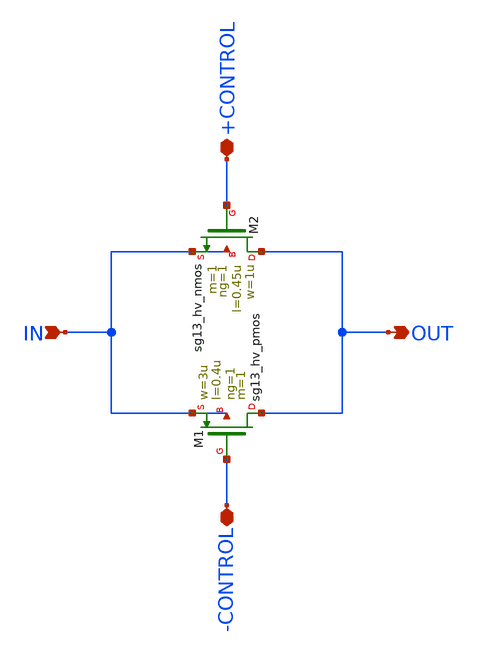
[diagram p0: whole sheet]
** sch_path: real_circuit/real_switch.sch
**.subckt real_switch IN OUT +CONTROL -CONTROL
*.ipin IN
*.opin OUT
*.iopin +CONTROL
*.iopin -CONTROL
XM1 OUT -CONTROL IN IN sg13_hv_pmos w=3u l=0.4u ng=1 m=1 mm_ok=1
XM2 OUT +CONTROL IN IN sg13_hv_nmos w=1u l=0.45u ng=1 m=1 mm_ok=1
**.ends
.end
